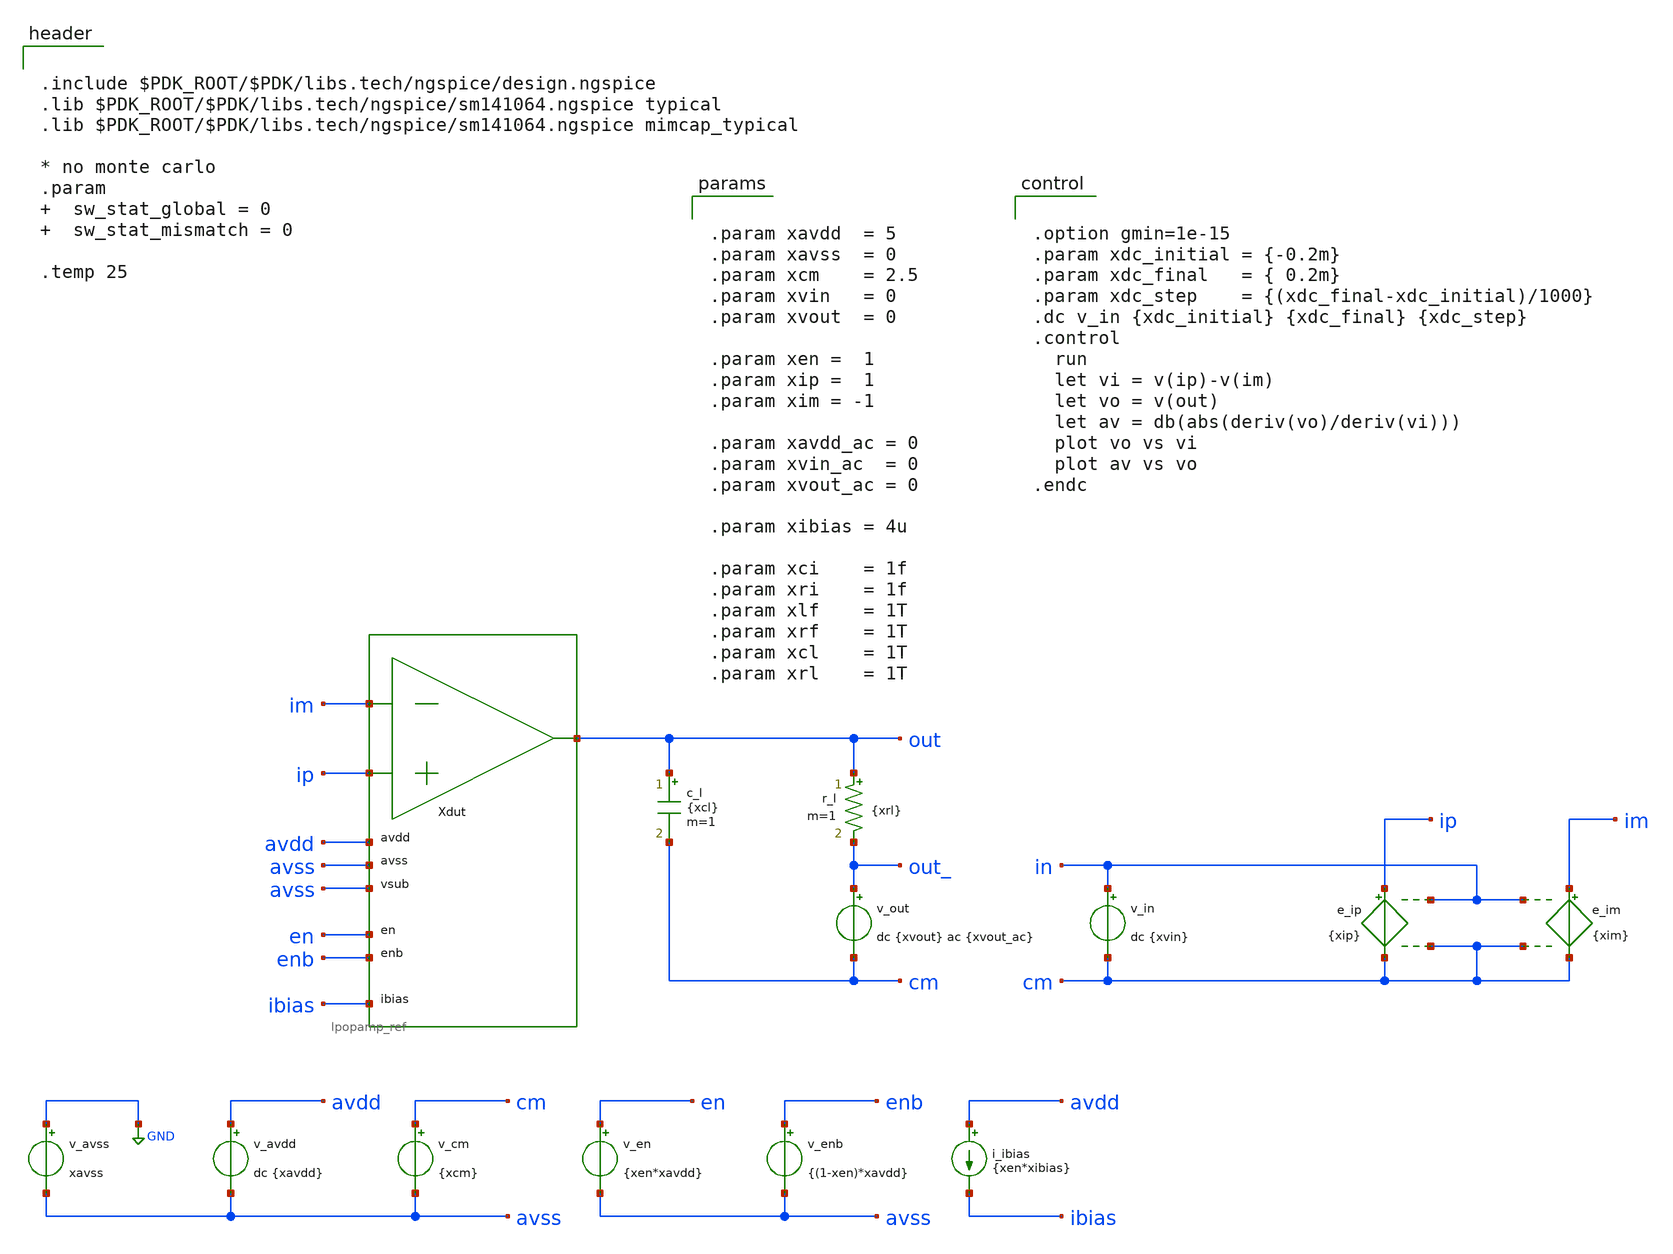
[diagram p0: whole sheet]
** sch_path: xschem/tb_lpopamp_open_dc.sch
**.subckt tb_lpopamp_open_dc
Xdut im ip out avdd avss avss en enb ibias lpopamp_ref
v_avss GND avss xavss
v_avdd avdd avss dc {xavdd}
v_in in cm dc {xvin}
v_en en avss {xen*xavdd}
v_enb enb avss {(1-xen)*xavdd}
i_ibias avdd ibias {xen*xibias}
c_l out cm {xcl} m=1
v_out out_ cm dc {xvout} ac {xvout_ac}
r_l out out_ {xrl} m=1
e_ip ip cm in cm {xip}
e_im im cm in cm {xim}
v_cm cm avss {xcm}
**** begin user architecture code


.include $PDK_ROOT/$PDK/libs.tech/ngspice/design.ngspice
.lib $PDK_ROOT/$PDK/libs.tech/ngspice/sm141064.ngspice typical
.lib $PDK_ROOT/$PDK/libs.tech/ngspice/sm141064.ngspice mimcap_typical

* no monte carlo
.param   sw_stat_global = 0   sw_stat_mismatch = 0

.temp 25





.option gmin=1e-15
.param xdc_initial = {-0.2m}
.param xdc_final   = { 0.2m}
.param xdc_step    = {(xdc_final-xdc_initial)/1000}
.dc v_in {xdc_initial} {xdc_final} {xdc_step}
.control
  run
  let vi = v(ip)-v(im)
  let vo = v(out)
  let av = db(abs(deriv(vo)/deriv(vi)))
  plot vo vs vi
  plot av vs vo
.endc




.param xavdd  = 5
.param xavss  = 0
.param xcm    = 2.5
.param xvin   = 0
.param xvout  = 0

.param xen =  1
.param xip =  1
.param xim = -1

.param xavdd_ac = 0
.param xvin_ac  = 0
.param xvout_ac = 0

.param xibias = 4u

.param xci    = 1f
.param xri    = 1f
.param xlf    = 1T
.param xrf    = 1T
.param xcl    = 1T
.param xrl    = 1T


**** end user architecture code
**.ends
.GLOBAL GND
.end
